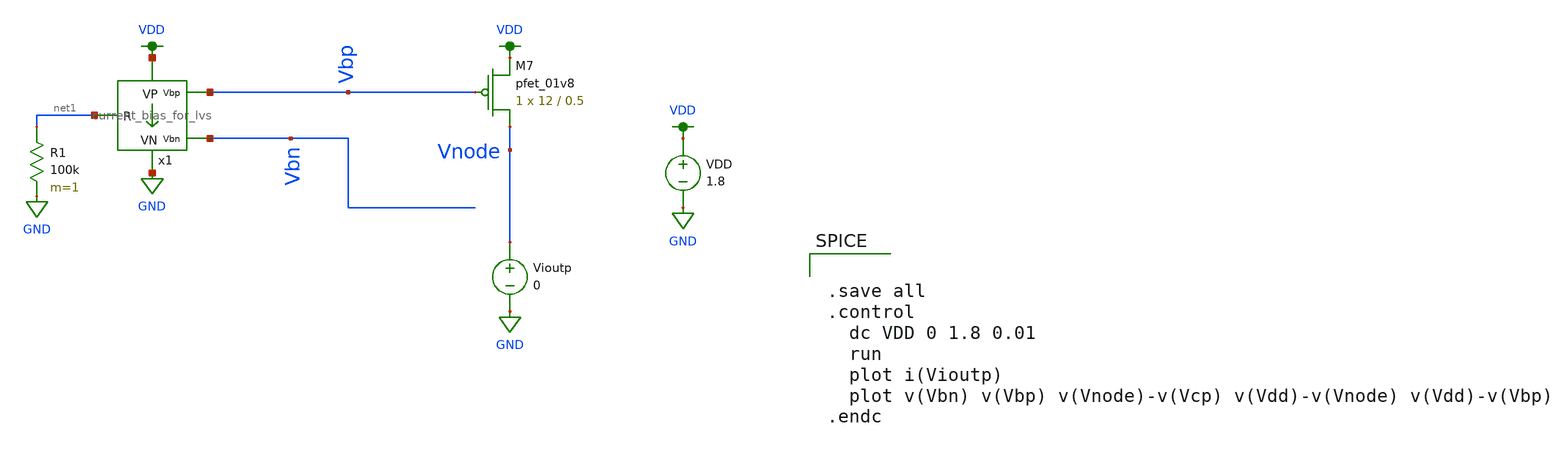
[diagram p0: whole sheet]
** sch_path: schematics/bias/test_lvs_current_bias_2.sch
**.subckt test_lvs_current_bias_2
VDD VDD GND 1.8
Vioutp Vnode GND 0
R1 net1 GND 100k m=1
x1 VDD GND Vbp Vbn net1 current_bias_for_lvs
XM7 Vnode Vbp VDD VDD sky130_fd_pr__pfet_01v8 L=0.5 W=12 nf=1 ad='int((nf+1)/2) * W/nf * 0.29' as='int((nf+2)/2) * W/nf * 0.29'
+ pd='2*int((nf+1)/2) * (W/nf + 0.29)' ps='2*int((nf+2)/2) * (W/nf + 0.29)' nrd='0.29 / W' nrs='0.29 / W'
+ sa=0 sb=0 sd=0 mult=1 m=1
**** begin user architecture code

.option wnflag=1
.param MC_SWITCH=0.0
.lib ~/skywater/skywater-pdk/libraries/sky130_fd_pr_ngspice/latest/models/sky130.lib.spice tt



.save all
.control
  dc VDD 0 1.8 0.01
  run
  plot i(Vioutp)
  plot v(Vbn) v(Vbp) v(Vnode)-v(Vcp) v(Vdd)-v(Vnode) v(Vdd)-v(Vbp)
.endc

**** end user architecture code
**.ends
.GLOBAL VDD
.GLOBAL GND
.end
